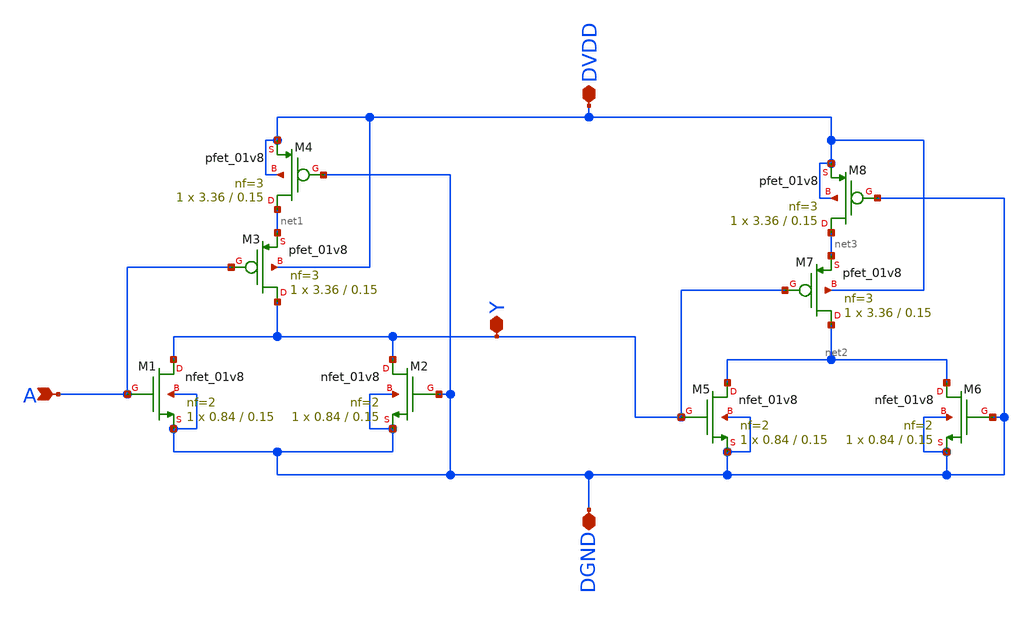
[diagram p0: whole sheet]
** sch_path: tutorial_7/nors.sch
**.subckt nors A DVDD DGND Y
*.ipin A
*.iopin DVDD
*.iopin DGND
*.iopin Y
XM1 Y A DGND DGND sky130_fd_pr__nfet_01v8 L=0.15 W=0.84 nf=2 ad='int((nf+1)/2) * W/nf * 0.29' as='int((nf+2)/2) * W/nf * 0.29'
+ pd='2*int((nf+1)/2) * (W/nf + 0.29)' ps='2*int((nf+2)/2) * (W/nf + 0.29)' nrd='0.29 / W' nrs='0.29 / W'
+ sa=0 sb=0 sd=0 mult=1 m=1
XM2 Y DGND DGND DGND sky130_fd_pr__nfet_01v8 L=0.15 W=0.84 nf=2 ad='int((nf+1)/2) * W/nf * 0.29' as='int((nf+2)/2) * W/nf * 0.29'
+ pd='2*int((nf+1)/2) * (W/nf + 0.29)' ps='2*int((nf+2)/2) * (W/nf + 0.29)' nrd='0.29 / W' nrs='0.29 / W'
+ sa=0 sb=0 sd=0 mult=1 m=1
XM3 Y A net1 DVDD sky130_fd_pr__pfet_01v8 L=0.15 W=3.36 nf=3 ad='int((nf+1)/2) * W/nf * 0.29' as='int((nf+2)/2) * W/nf * 0.29'
+ pd='2*int((nf+1)/2) * (W/nf + 0.29)' ps='2*int((nf+2)/2) * (W/nf + 0.29)' nrd='0.29 / W' nrs='0.29 / W'
+ sa=0 sb=0 sd=0 mult=1 m=1
XM4 net1 DGND DVDD DVDD sky130_fd_pr__pfet_01v8 L=0.15 W=3.36 nf=3 ad='int((nf+1)/2) * W/nf * 0.29' as='int((nf+2)/2) * W/nf * 0.29'
+ pd='2*int((nf+1)/2) * (W/nf + 0.29)' ps='2*int((nf+2)/2) * (W/nf + 0.29)' nrd='0.29 / W' nrs='0.29 / W'
+ sa=0 sb=0 sd=0 mult=1 m=1
XM5 net2 Y DGND DGND sky130_fd_pr__nfet_01v8 L=0.15 W=0.84 nf=2 ad='int((nf+1)/2) * W/nf * 0.29' as='int((nf+2)/2) * W/nf * 0.29'
+ pd='2*int((nf+1)/2) * (W/nf + 0.29)' ps='2*int((nf+2)/2) * (W/nf + 0.29)' nrd='0.29 / W' nrs='0.29 / W'
+ sa=0 sb=0 sd=0 mult=1 m=1
XM6 net2 DGND DGND DGND sky130_fd_pr__nfet_01v8 L=0.15 W=0.84 nf=2 ad='int((nf+1)/2) * W/nf * 0.29' as='int((nf+2)/2) * W/nf * 0.29'
+ pd='2*int((nf+1)/2) * (W/nf + 0.29)' ps='2*int((nf+2)/2) * (W/nf + 0.29)' nrd='0.29 / W' nrs='0.29 / W'
+ sa=0 sb=0 sd=0 mult=1 m=1
XM7 net2 Y net3 DVDD sky130_fd_pr__pfet_01v8 L=0.15 W=3.36 nf=3 ad='int((nf+1)/2) * W/nf * 0.29' as='int((nf+2)/2) * W/nf * 0.29'
+ pd='2*int((nf+1)/2) * (W/nf + 0.29)' ps='2*int((nf+2)/2) * (W/nf + 0.29)' nrd='0.29 / W' nrs='0.29 / W'
+ sa=0 sb=0 sd=0 mult=1 m=1
XM8 net3 DGND DVDD DVDD sky130_fd_pr__pfet_01v8 L=0.15 W=3.36 nf=3 ad='int((nf+1)/2) * W/nf * 0.29' as='int((nf+2)/2) * W/nf * 0.29'
+ pd='2*int((nf+1)/2) * (W/nf + 0.29)' ps='2*int((nf+2)/2) * (W/nf + 0.29)' nrd='0.29 / W' nrs='0.29 / W'
+ sa=0 sb=0 sd=0 mult=1 m=1
**.ends
.end
